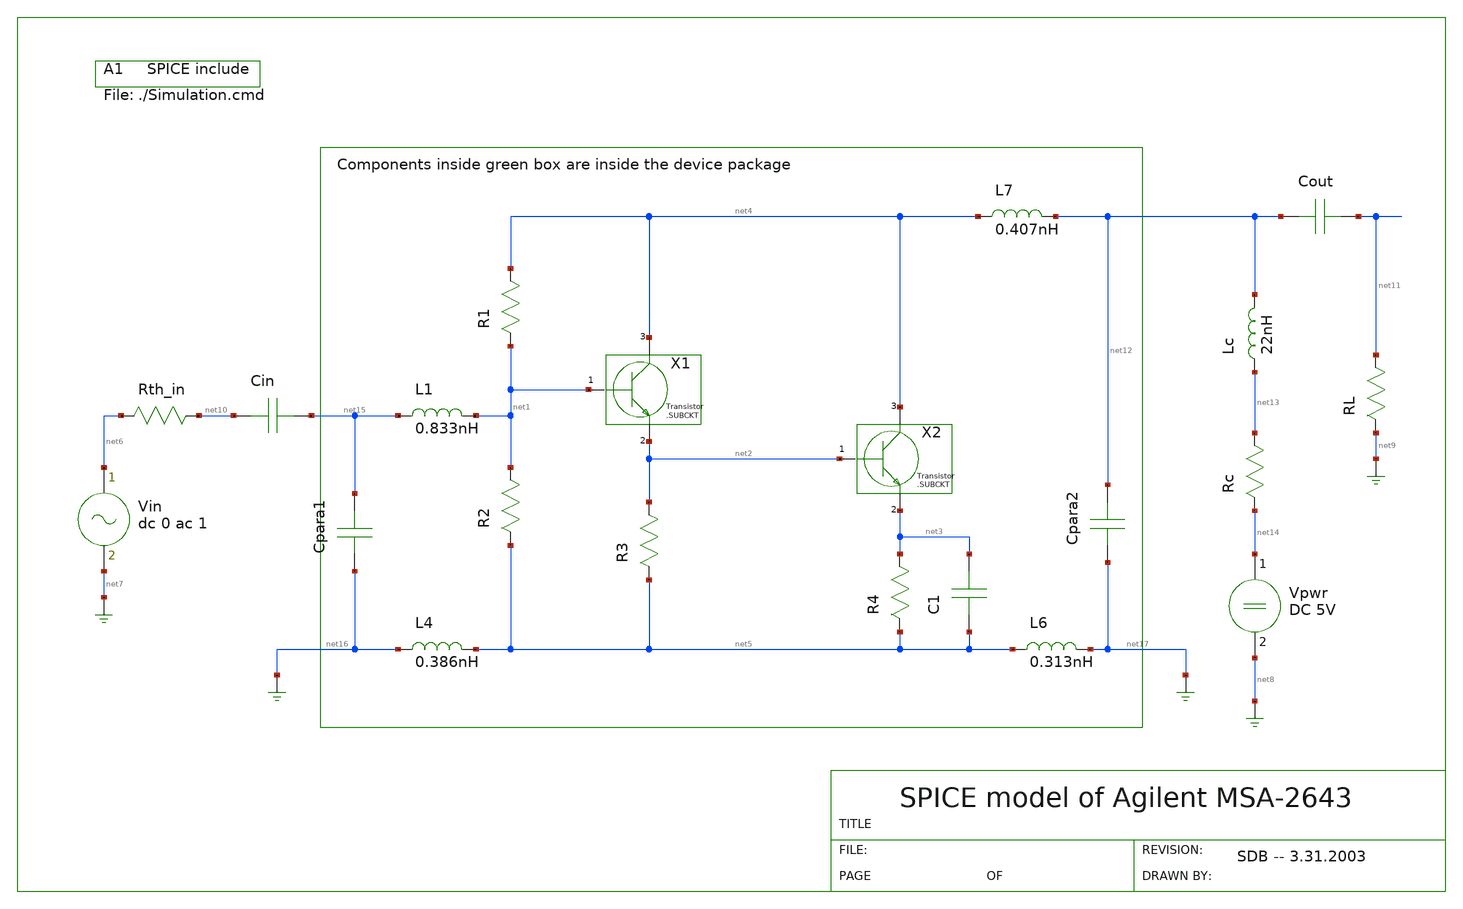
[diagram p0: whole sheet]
** sch_path: xschem_library/gschem_import/MSA-2643.sch
**.subckt MSA-2643
R1 net4 net1 560
R2 net1 net5 660
R3 net2 net5 250
R4 net3 net5 5
X1 net4 net1 net2
X2 net4 net2 net3
C1 net5 net3 4pF
Vpwr net14 net8 DC 5V
Vin net6 net7 dc 0 ac 1
Rth_in net10 net6 50
RL net11 net9 50
Lc net13 net12 22nH
Rc net13 net14 50
Cout net12 net11 47pF
Cin net10 net15 47pF
.include ./Simulation.cmd
L4 net16 net5 0.386nH
L6 net5 net17 0.313nH
L1 net15 net1 0.833nH
L7 net4 net12 0.407nH
Cpara1 net16 net15 0.158pF
Cpara2 net17 net12 0.155pF
**.ends
.end
